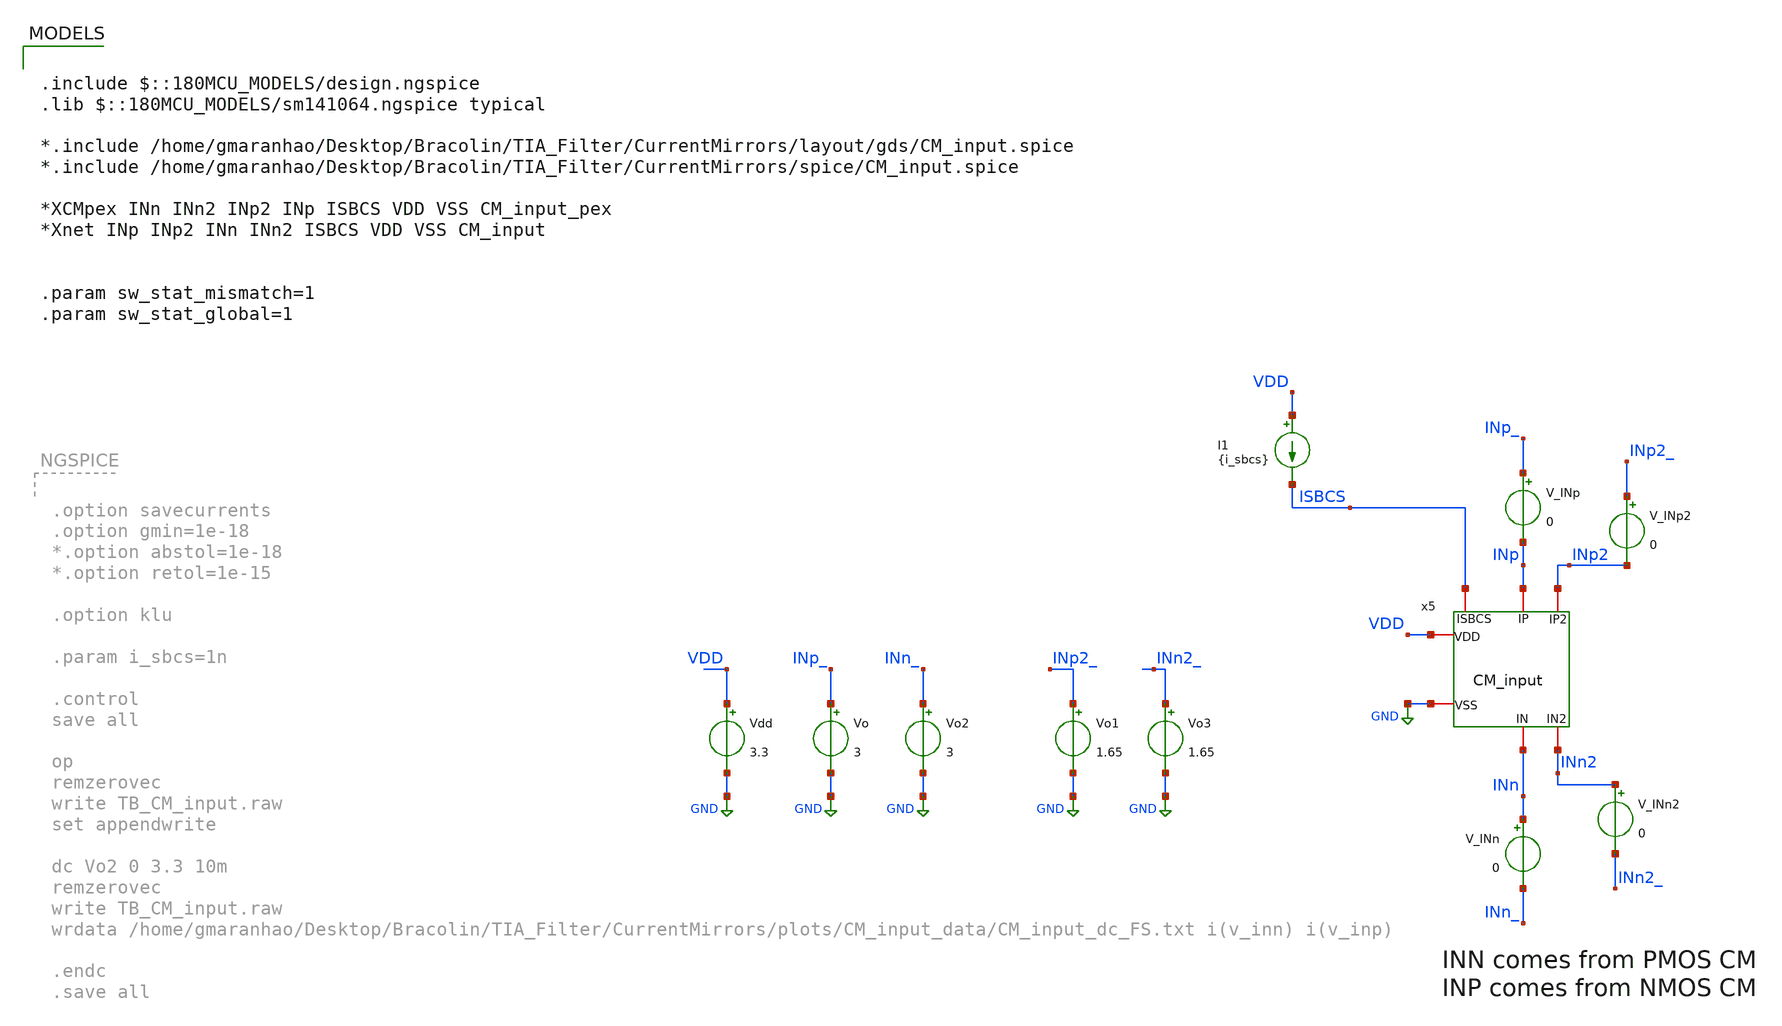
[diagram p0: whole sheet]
** sch_path: TIA_Filter/CurrentMirrors/TB_CM_input.sch
**.subckt TB_CM_input
I1 VDD ISBCS {i_sbcs}
x5 INp INp2 INn INn2 ISBCS VDD GND CM_input
Vdd VDD GND 3.3
Vo INp_ GND 3
Vo1 INp2_ GND 1.65
Vo2 INn_ GND 3
Vo3 INn2_ GND 1.65
V_INp INp_ INp 0
V_INp2 INp2_ INp2 0
V_INn INn INn_ 0
V_INn2 INn2 INn2_ 0
**** begin user architecture code

.include $::180MCU_MODELS/design.ngspice
.lib $::180MCU_MODELS/sm141064.ngspice typical

*.include /home/gmaranhao/Desktop/Bracolin/TIA_Filter/CurrentMirrors/layout/gds/CM_input.spice
*.include /home/gmaranhao/Desktop/Bracolin/TIA_Filter/CurrentMirrors/spice/CM_input.spice

*XCMpex INn INn2 INp2 INp ISBCS VDD VSS CM_input_pex
*Xnet INp INp2 INn INn2 ISBCS VDD VSS CM_input


.param sw_stat_mismatch=1
.param sw_stat_global=1




.option gmin=1e-15
*.option abstol=1e-18
*.option retol=1e-15

.option klu

.param i_sbcs=1n

.control
save all

let sample_num = 0

while sample_num<203
reset

*dc Vo 0 3.3 10m
op
remzerovec
write TB_CM_input.raw
wrdata
+ /home/gmaranhao/Desktop/Bracolin/TIA_Filter/CurrentMirrors/plots/CM_input_data/CM_input_dc_MisMC_3p0.txt i(v_inn) i(v_inp)
set appendwrite

let sample_num = sample_num + 1
end


.endc
.save all


**** end user architecture code
**.ends

* expanding   symbol:  CurrentMirrors/CM_input.sym # of pins=7
** sym_path: TIA_Filter/CurrentMirrors/CM_input.sym
** sch_path: TIA_Filter/CurrentMirrors/CM_input.sch
.subckt CM_input IP IP2 IN IN2 ISBCS VDD VSS
*.iopin IP
*.iopin IP2
*.iopin IN
*.iopin IN2
*.iopin ISBCS
*.iopin VDD
*.iopin VSS
XM1[1] ISBCS ISBCS net1[1] VSS nfet_03v3 L=6u W=2u nf=1 ad='int((nf+1)/2) * W/nf * 0.18u' as='int((nf+2)/2) * W/nf * 0.18u'
+ pd='2*int((nf+1)/2) * (W/nf + 0.18u)' ps='2*int((nf+2)/2) * (W/nf + 0.18u)' nrd='0.18u / W' nrs='0.18u / W'
+ sa=0 sb=0 sd=0 m=1
XM1[2] ISBCS ISBCS net1[0] VSS nfet_03v3 L=6u W=2u nf=1 ad='int((nf+1)/2) * W/nf * 0.18u' as='int((nf+2)/2) * W/nf * 0.18u'
+ pd='2*int((nf+1)/2) * (W/nf + 0.18u)' ps='2*int((nf+2)/2) * (W/nf + 0.18u)' nrd='0.18u / W' nrs='0.18u / W'
+ sa=0 sb=0 sd=0 m=1
XM2[1] vgp vgp net5[1] VDD pfet_03v3 L=6u W=2u nf=1 ad='int((nf+1)/2) * W/nf * 0.18u' as='int((nf+2)/2) * W/nf * 0.18u'
+ pd='2*int((nf+1)/2) * (W/nf + 0.18u)' ps='2*int((nf+2)/2) * (W/nf + 0.18u)' nrd='0.18u / W' nrs='0.18u / W'
+ sa=0 sb=0 sd=0 m=1
XM2[2] vgp vgp net5[0] VDD pfet_03v3 L=6u W=2u nf=1 ad='int((nf+1)/2) * W/nf * 0.18u' as='int((nf+2)/2) * W/nf * 0.18u'
+ pd='2*int((nf+1)/2) * (W/nf + 0.18u)' ps='2*int((nf+2)/2) * (W/nf + 0.18u)' nrd='0.18u / W' nrs='0.18u / W'
+ sa=0 sb=0 sd=0 m=1
XM3[1] net1[1] ISBCS VSS VSS nfet_03v3 L=6u W=2u nf=1 ad='int((nf+1)/2) * W/nf * 0.18u' as='int((nf+2)/2) * W/nf * 0.18u'
+ pd='2*int((nf+1)/2) * (W/nf + 0.18u)' ps='2*int((nf+2)/2) * (W/nf + 0.18u)' nrd='0.18u / W' nrs='0.18u / W'
+ sa=0 sb=0 sd=0 m=1
XM3[2] net1[0] ISBCS VSS VSS nfet_03v3 L=6u W=2u nf=1 ad='int((nf+1)/2) * W/nf * 0.18u' as='int((nf+2)/2) * W/nf * 0.18u'
+ pd='2*int((nf+1)/2) * (W/nf + 0.18u)' ps='2*int((nf+2)/2) * (W/nf + 0.18u)' nrd='0.18u / W' nrs='0.18u / W'
+ sa=0 sb=0 sd=0 m=1
XM4[1] IP ISBCS net2[1] VSS nfet_03v3 L=6u W=2u nf=1 ad='int((nf+1)/2) * W/nf * 0.18u' as='int((nf+2)/2) * W/nf * 0.18u'
+ pd='2*int((nf+1)/2) * (W/nf + 0.18u)' ps='2*int((nf+2)/2) * (W/nf + 0.18u)' nrd='0.18u / W' nrs='0.18u / W'
+ sa=0 sb=0 sd=0 m=1
XM4[2] IP ISBCS net2[0] VSS nfet_03v3 L=6u W=2u nf=1 ad='int((nf+1)/2) * W/nf * 0.18u' as='int((nf+2)/2) * W/nf * 0.18u'
+ pd='2*int((nf+1)/2) * (W/nf + 0.18u)' ps='2*int((nf+2)/2) * (W/nf + 0.18u)' nrd='0.18u / W' nrs='0.18u / W'
+ sa=0 sb=0 sd=0 m=1
XM5[1] net2[1] ISBCS VSS VSS nfet_03v3 L=6u W=2u nf=1 ad='int((nf+1)/2) * W/nf * 0.18u' as='int((nf+2)/2) * W/nf * 0.18u'
+ pd='2*int((nf+1)/2) * (W/nf + 0.18u)' ps='2*int((nf+2)/2) * (W/nf + 0.18u)' nrd='0.18u / W' nrs='0.18u / W'
+ sa=0 sb=0 sd=0 m=1
XM5[2] net2[0] ISBCS VSS VSS nfet_03v3 L=6u W=2u nf=1 ad='int((nf+1)/2) * W/nf * 0.18u' as='int((nf+2)/2) * W/nf * 0.18u'
+ pd='2*int((nf+1)/2) * (W/nf + 0.18u)' ps='2*int((nf+2)/2) * (W/nf + 0.18u)' nrd='0.18u / W' nrs='0.18u / W'
+ sa=0 sb=0 sd=0 m=1
XM6[1] IP2 ISBCS net3[1] VSS nfet_03v3 L=6u W=2u nf=1 ad='int((nf+1)/2) * W/nf * 0.18u' as='int((nf+2)/2) * W/nf * 0.18u'
+ pd='2*int((nf+1)/2) * (W/nf + 0.18u)' ps='2*int((nf+2)/2) * (W/nf + 0.18u)' nrd='0.18u / W' nrs='0.18u / W'
+ sa=0 sb=0 sd=0 m=1
XM6[2] IP2 ISBCS net3[0] VSS nfet_03v3 L=6u W=2u nf=1 ad='int((nf+1)/2) * W/nf * 0.18u' as='int((nf+2)/2) * W/nf * 0.18u'
+ pd='2*int((nf+1)/2) * (W/nf + 0.18u)' ps='2*int((nf+2)/2) * (W/nf + 0.18u)' nrd='0.18u / W' nrs='0.18u / W'
+ sa=0 sb=0 sd=0 m=1
XM7[1] net3[1] ISBCS VSS VSS nfet_03v3 L=6u W=2u nf=1 ad='int((nf+1)/2) * W/nf * 0.18u' as='int((nf+2)/2) * W/nf * 0.18u'
+ pd='2*int((nf+1)/2) * (W/nf + 0.18u)' ps='2*int((nf+2)/2) * (W/nf + 0.18u)' nrd='0.18u / W' nrs='0.18u / W'
+ sa=0 sb=0 sd=0 m=1
XM7[2] net3[0] ISBCS VSS VSS nfet_03v3 L=6u W=2u nf=1 ad='int((nf+1)/2) * W/nf * 0.18u' as='int((nf+2)/2) * W/nf * 0.18u'
+ pd='2*int((nf+1)/2) * (W/nf + 0.18u)' ps='2*int((nf+2)/2) * (W/nf + 0.18u)' nrd='0.18u / W' nrs='0.18u / W'
+ sa=0 sb=0 sd=0 m=1
XM8[1] vgp ISBCS net4[1] VSS nfet_03v3 L=6u W=2u nf=1 ad='int((nf+1)/2) * W/nf * 0.18u' as='int((nf+2)/2) * W/nf * 0.18u'
+ pd='2*int((nf+1)/2) * (W/nf + 0.18u)' ps='2*int((nf+2)/2) * (W/nf + 0.18u)' nrd='0.18u / W' nrs='0.18u / W'
+ sa=0 sb=0 sd=0 m=1
XM8[2] vgp ISBCS net4[0] VSS nfet_03v3 L=6u W=2u nf=1 ad='int((nf+1)/2) * W/nf * 0.18u' as='int((nf+2)/2) * W/nf * 0.18u'
+ pd='2*int((nf+1)/2) * (W/nf + 0.18u)' ps='2*int((nf+2)/2) * (W/nf + 0.18u)' nrd='0.18u / W' nrs='0.18u / W'
+ sa=0 sb=0 sd=0 m=1
XM9[1] net4[1] ISBCS VSS VSS nfet_03v3 L=6u W=2u nf=1 ad='int((nf+1)/2) * W/nf * 0.18u' as='int((nf+2)/2) * W/nf * 0.18u'
+ pd='2*int((nf+1)/2) * (W/nf + 0.18u)' ps='2*int((nf+2)/2) * (W/nf + 0.18u)' nrd='0.18u / W' nrs='0.18u / W'
+ sa=0 sb=0 sd=0 m=1
XM9[2] net4[0] ISBCS VSS VSS nfet_03v3 L=6u W=2u nf=1 ad='int((nf+1)/2) * W/nf * 0.18u' as='int((nf+2)/2) * W/nf * 0.18u'
+ pd='2*int((nf+1)/2) * (W/nf + 0.18u)' ps='2*int((nf+2)/2) * (W/nf + 0.18u)' nrd='0.18u / W' nrs='0.18u / W'
+ sa=0 sb=0 sd=0 m=1
XM10[1] net5[1] vgp VDD VDD pfet_03v3 L=6u W=2u nf=1 ad='int((nf+1)/2) * W/nf * 0.18u' as='int((nf+2)/2) * W/nf * 0.18u'
+ pd='2*int((nf+1)/2) * (W/nf + 0.18u)' ps='2*int((nf+2)/2) * (W/nf + 0.18u)' nrd='0.18u / W' nrs='0.18u / W'
+ sa=0 sb=0 sd=0 m=1
XM10[2] net5[0] vgp VDD VDD pfet_03v3 L=6u W=2u nf=1 ad='int((nf+1)/2) * W/nf * 0.18u' as='int((nf+2)/2) * W/nf * 0.18u'
+ pd='2*int((nf+1)/2) * (W/nf + 0.18u)' ps='2*int((nf+2)/2) * (W/nf + 0.18u)' nrd='0.18u / W' nrs='0.18u / W'
+ sa=0 sb=0 sd=0 m=1
XM11[1] IN vgp net6[1] VDD pfet_03v3 L=6u W=2u nf=1 ad='int((nf+1)/2) * W/nf * 0.18u' as='int((nf+2)/2) * W/nf * 0.18u'
+ pd='2*int((nf+1)/2) * (W/nf + 0.18u)' ps='2*int((nf+2)/2) * (W/nf + 0.18u)' nrd='0.18u / W' nrs='0.18u / W'
+ sa=0 sb=0 sd=0 m=1
XM11[2] IN vgp net6[0] VDD pfet_03v3 L=6u W=2u nf=1 ad='int((nf+1)/2) * W/nf * 0.18u' as='int((nf+2)/2) * W/nf * 0.18u'
+ pd='2*int((nf+1)/2) * (W/nf + 0.18u)' ps='2*int((nf+2)/2) * (W/nf + 0.18u)' nrd='0.18u / W' nrs='0.18u / W'
+ sa=0 sb=0 sd=0 m=1
XM12[1] net6[1] vgp VDD VDD pfet_03v3 L=6u W=2u nf=1 ad='int((nf+1)/2) * W/nf * 0.18u' as='int((nf+2)/2) * W/nf * 0.18u'
+ pd='2*int((nf+1)/2) * (W/nf + 0.18u)' ps='2*int((nf+2)/2) * (W/nf + 0.18u)' nrd='0.18u / W' nrs='0.18u / W'
+ sa=0 sb=0 sd=0 m=1
XM12[2] net6[0] vgp VDD VDD pfet_03v3 L=6u W=2u nf=1 ad='int((nf+1)/2) * W/nf * 0.18u' as='int((nf+2)/2) * W/nf * 0.18u'
+ pd='2*int((nf+1)/2) * (W/nf + 0.18u)' ps='2*int((nf+2)/2) * (W/nf + 0.18u)' nrd='0.18u / W' nrs='0.18u / W'
+ sa=0 sb=0 sd=0 m=1
XM13[1] IN2 vgp net7[1] VDD pfet_03v3 L=6u W=2u nf=1 ad='int((nf+1)/2) * W/nf * 0.18u' as='int((nf+2)/2) * W/nf * 0.18u'
+ pd='2*int((nf+1)/2) * (W/nf + 0.18u)' ps='2*int((nf+2)/2) * (W/nf + 0.18u)' nrd='0.18u / W' nrs='0.18u / W'
+ sa=0 sb=0 sd=0 m=1
XM13[2] IN2 vgp net7[0] VDD pfet_03v3 L=6u W=2u nf=1 ad='int((nf+1)/2) * W/nf * 0.18u' as='int((nf+2)/2) * W/nf * 0.18u'
+ pd='2*int((nf+1)/2) * (W/nf + 0.18u)' ps='2*int((nf+2)/2) * (W/nf + 0.18u)' nrd='0.18u / W' nrs='0.18u / W'
+ sa=0 sb=0 sd=0 m=1
XM16[1] net7[1] vgp VDD VDD pfet_03v3 L=6u W=2u nf=1 ad='int((nf+1)/2) * W/nf * 0.18u' as='int((nf+2)/2) * W/nf * 0.18u'
+ pd='2*int((nf+1)/2) * (W/nf + 0.18u)' ps='2*int((nf+2)/2) * (W/nf + 0.18u)' nrd='0.18u / W' nrs='0.18u / W'
+ sa=0 sb=0 sd=0 m=1
XM16[2] net7[0] vgp VDD VDD pfet_03v3 L=6u W=2u nf=1 ad='int((nf+1)/2) * W/nf * 0.18u' as='int((nf+2)/2) * W/nf * 0.18u'
+ pd='2*int((nf+1)/2) * (W/nf + 0.18u)' ps='2*int((nf+2)/2) * (W/nf + 0.18u)' nrd='0.18u / W' nrs='0.18u / W'
+ sa=0 sb=0 sd=0 m=1
XM14[1] VSS VSS VSS VSS nfet_03v3 L=6u W=2u nf=1 ad='int((nf+1)/2) * W/nf * 0.18u' as='int((nf+2)/2) * W/nf * 0.18u'
+ pd='2*int((nf+1)/2) * (W/nf + 0.18u)' ps='2*int((nf+2)/2) * (W/nf + 0.18u)' nrd='0.18u / W' nrs='0.18u / W'
+ sa=0 sb=0 sd=0 m=1
XM14[2] VSS VSS VSS VSS nfet_03v3 L=6u W=2u nf=1 ad='int((nf+1)/2) * W/nf * 0.18u' as='int((nf+2)/2) * W/nf * 0.18u'
+ pd='2*int((nf+1)/2) * (W/nf + 0.18u)' ps='2*int((nf+2)/2) * (W/nf + 0.18u)' nrd='0.18u / W' nrs='0.18u / W'
+ sa=0 sb=0 sd=0 m=1
XM14[3] VSS VSS VSS VSS nfet_03v3 L=6u W=2u nf=1 ad='int((nf+1)/2) * W/nf * 0.18u' as='int((nf+2)/2) * W/nf * 0.18u'
+ pd='2*int((nf+1)/2) * (W/nf + 0.18u)' ps='2*int((nf+2)/2) * (W/nf + 0.18u)' nrd='0.18u / W' nrs='0.18u / W'
+ sa=0 sb=0 sd=0 m=1
XM14[4] VSS VSS VSS VSS nfet_03v3 L=6u W=2u nf=1 ad='int((nf+1)/2) * W/nf * 0.18u' as='int((nf+2)/2) * W/nf * 0.18u'
+ pd='2*int((nf+1)/2) * (W/nf + 0.18u)' ps='2*int((nf+2)/2) * (W/nf + 0.18u)' nrd='0.18u / W' nrs='0.18u / W'
+ sa=0 sb=0 sd=0 m=1
XM14[5] VSS VSS VSS VSS nfet_03v3 L=6u W=2u nf=1 ad='int((nf+1)/2) * W/nf * 0.18u' as='int((nf+2)/2) * W/nf * 0.18u'
+ pd='2*int((nf+1)/2) * (W/nf + 0.18u)' ps='2*int((nf+2)/2) * (W/nf + 0.18u)' nrd='0.18u / W' nrs='0.18u / W'
+ sa=0 sb=0 sd=0 m=1
XM14[6] VSS VSS VSS VSS nfet_03v3 L=6u W=2u nf=1 ad='int((nf+1)/2) * W/nf * 0.18u' as='int((nf+2)/2) * W/nf * 0.18u'
+ pd='2*int((nf+1)/2) * (W/nf + 0.18u)' ps='2*int((nf+2)/2) * (W/nf + 0.18u)' nrd='0.18u / W' nrs='0.18u / W'
+ sa=0 sb=0 sd=0 m=1
XM14[7] VSS VSS VSS VSS nfet_03v3 L=6u W=2u nf=1 ad='int((nf+1)/2) * W/nf * 0.18u' as='int((nf+2)/2) * W/nf * 0.18u'
+ pd='2*int((nf+1)/2) * (W/nf + 0.18u)' ps='2*int((nf+2)/2) * (W/nf + 0.18u)' nrd='0.18u / W' nrs='0.18u / W'
+ sa=0 sb=0 sd=0 m=1
XM14[8] VSS VSS VSS VSS nfet_03v3 L=6u W=2u nf=1 ad='int((nf+1)/2) * W/nf * 0.18u' as='int((nf+2)/2) * W/nf * 0.18u'
+ pd='2*int((nf+1)/2) * (W/nf + 0.18u)' ps='2*int((nf+2)/2) * (W/nf + 0.18u)' nrd='0.18u / W' nrs='0.18u / W'
+ sa=0 sb=0 sd=0 m=1
XM14[9] VSS VSS VSS VSS nfet_03v3 L=6u W=2u nf=1 ad='int((nf+1)/2) * W/nf * 0.18u' as='int((nf+2)/2) * W/nf * 0.18u'
+ pd='2*int((nf+1)/2) * (W/nf + 0.18u)' ps='2*int((nf+2)/2) * (W/nf + 0.18u)' nrd='0.18u / W' nrs='0.18u / W'
+ sa=0 sb=0 sd=0 m=1
XM14[10] VSS VSS VSS VSS nfet_03v3 L=6u W=2u nf=1 ad='int((nf+1)/2) * W/nf * 0.18u' as='int((nf+2)/2) * W/nf * 0.18u'
+ pd='2*int((nf+1)/2) * (W/nf + 0.18u)' ps='2*int((nf+2)/2) * (W/nf + 0.18u)' nrd='0.18u / W' nrs='0.18u / W'
+ sa=0 sb=0 sd=0 m=1
XM14[11] VSS VSS VSS VSS nfet_03v3 L=6u W=2u nf=1 ad='int((nf+1)/2) * W/nf * 0.18u' as='int((nf+2)/2) * W/nf * 0.18u'
+ pd='2*int((nf+1)/2) * (W/nf + 0.18u)' ps='2*int((nf+2)/2) * (W/nf + 0.18u)' nrd='0.18u / W' nrs='0.18u / W'
+ sa=0 sb=0 sd=0 m=1
XM14[12] VSS VSS VSS VSS nfet_03v3 L=6u W=2u nf=1 ad='int((nf+1)/2) * W/nf * 0.18u' as='int((nf+2)/2) * W/nf * 0.18u'
+ pd='2*int((nf+1)/2) * (W/nf + 0.18u)' ps='2*int((nf+2)/2) * (W/nf + 0.18u)' nrd='0.18u / W' nrs='0.18u / W'
+ sa=0 sb=0 sd=0 m=1
XM14[13] VSS VSS VSS VSS nfet_03v3 L=6u W=2u nf=1 ad='int((nf+1)/2) * W/nf * 0.18u' as='int((nf+2)/2) * W/nf * 0.18u'
+ pd='2*int((nf+1)/2) * (W/nf + 0.18u)' ps='2*int((nf+2)/2) * (W/nf + 0.18u)' nrd='0.18u / W' nrs='0.18u / W'
+ sa=0 sb=0 sd=0 m=1
XM14[14] VSS VSS VSS VSS nfet_03v3 L=6u W=2u nf=1 ad='int((nf+1)/2) * W/nf * 0.18u' as='int((nf+2)/2) * W/nf * 0.18u'
+ pd='2*int((nf+1)/2) * (W/nf + 0.18u)' ps='2*int((nf+2)/2) * (W/nf + 0.18u)' nrd='0.18u / W' nrs='0.18u / W'
+ sa=0 sb=0 sd=0 m=1
XM14[15] VSS VSS VSS VSS nfet_03v3 L=6u W=2u nf=1 ad='int((nf+1)/2) * W/nf * 0.18u' as='int((nf+2)/2) * W/nf * 0.18u'
+ pd='2*int((nf+1)/2) * (W/nf + 0.18u)' ps='2*int((nf+2)/2) * (W/nf + 0.18u)' nrd='0.18u / W' nrs='0.18u / W'
+ sa=0 sb=0 sd=0 m=1
XM14[16] VSS VSS VSS VSS nfet_03v3 L=6u W=2u nf=1 ad='int((nf+1)/2) * W/nf * 0.18u' as='int((nf+2)/2) * W/nf * 0.18u'
+ pd='2*int((nf+1)/2) * (W/nf + 0.18u)' ps='2*int((nf+2)/2) * (W/nf + 0.18u)' nrd='0.18u / W' nrs='0.18u / W'
+ sa=0 sb=0 sd=0 m=1
XM14[17] VSS VSS VSS VSS nfet_03v3 L=6u W=2u nf=1 ad='int((nf+1)/2) * W/nf * 0.18u' as='int((nf+2)/2) * W/nf * 0.18u'
+ pd='2*int((nf+1)/2) * (W/nf + 0.18u)' ps='2*int((nf+2)/2) * (W/nf + 0.18u)' nrd='0.18u / W' nrs='0.18u / W'
+ sa=0 sb=0 sd=0 m=1
XM14[18] VSS VSS VSS VSS nfet_03v3 L=6u W=2u nf=1 ad='int((nf+1)/2) * W/nf * 0.18u' as='int((nf+2)/2) * W/nf * 0.18u'
+ pd='2*int((nf+1)/2) * (W/nf + 0.18u)' ps='2*int((nf+2)/2) * (W/nf + 0.18u)' nrd='0.18u / W' nrs='0.18u / W'
+ sa=0 sb=0 sd=0 m=1
XM14[19] VSS VSS VSS VSS nfet_03v3 L=6u W=2u nf=1 ad='int((nf+1)/2) * W/nf * 0.18u' as='int((nf+2)/2) * W/nf * 0.18u'
+ pd='2*int((nf+1)/2) * (W/nf + 0.18u)' ps='2*int((nf+2)/2) * (W/nf + 0.18u)' nrd='0.18u / W' nrs='0.18u / W'
+ sa=0 sb=0 sd=0 m=1
XM14[20] VSS VSS VSS VSS nfet_03v3 L=6u W=2u nf=1 ad='int((nf+1)/2) * W/nf * 0.18u' as='int((nf+2)/2) * W/nf * 0.18u'
+ pd='2*int((nf+1)/2) * (W/nf + 0.18u)' ps='2*int((nf+2)/2) * (W/nf + 0.18u)' nrd='0.18u / W' nrs='0.18u / W'
+ sa=0 sb=0 sd=0 m=1
XM15[1] VDD VDD VDD VDD pfet_03v3 L=6u W=2u nf=1 ad='int((nf+1)/2) * W/nf * 0.18u' as='int((nf+2)/2) * W/nf * 0.18u'
+ pd='2*int((nf+1)/2) * (W/nf + 0.18u)' ps='2*int((nf+2)/2) * (W/nf + 0.18u)' nrd='0.18u / W' nrs='0.18u / W'
+ sa=0 sb=0 sd=0 m=1
XM15[2] VDD VDD VDD VDD pfet_03v3 L=6u W=2u nf=1 ad='int((nf+1)/2) * W/nf * 0.18u' as='int((nf+2)/2) * W/nf * 0.18u'
+ pd='2*int((nf+1)/2) * (W/nf + 0.18u)' ps='2*int((nf+2)/2) * (W/nf + 0.18u)' nrd='0.18u / W' nrs='0.18u / W'
+ sa=0 sb=0 sd=0 m=1
XM15[3] VDD VDD VDD VDD pfet_03v3 L=6u W=2u nf=1 ad='int((nf+1)/2) * W/nf * 0.18u' as='int((nf+2)/2) * W/nf * 0.18u'
+ pd='2*int((nf+1)/2) * (W/nf + 0.18u)' ps='2*int((nf+2)/2) * (W/nf + 0.18u)' nrd='0.18u / W' nrs='0.18u / W'
+ sa=0 sb=0 sd=0 m=1
XM15[4] VDD VDD VDD VDD pfet_03v3 L=6u W=2u nf=1 ad='int((nf+1)/2) * W/nf * 0.18u' as='int((nf+2)/2) * W/nf * 0.18u'
+ pd='2*int((nf+1)/2) * (W/nf + 0.18u)' ps='2*int((nf+2)/2) * (W/nf + 0.18u)' nrd='0.18u / W' nrs='0.18u / W'
+ sa=0 sb=0 sd=0 m=1
XM15[5] VDD VDD VDD VDD pfet_03v3 L=6u W=2u nf=1 ad='int((nf+1)/2) * W/nf * 0.18u' as='int((nf+2)/2) * W/nf * 0.18u'
+ pd='2*int((nf+1)/2) * (W/nf + 0.18u)' ps='2*int((nf+2)/2) * (W/nf + 0.18u)' nrd='0.18u / W' nrs='0.18u / W'
+ sa=0 sb=0 sd=0 m=1
XM15[6] VDD VDD VDD VDD pfet_03v3 L=6u W=2u nf=1 ad='int((nf+1)/2) * W/nf * 0.18u' as='int((nf+2)/2) * W/nf * 0.18u'
+ pd='2*int((nf+1)/2) * (W/nf + 0.18u)' ps='2*int((nf+2)/2) * (W/nf + 0.18u)' nrd='0.18u / W' nrs='0.18u / W'
+ sa=0 sb=0 sd=0 m=1
XM15[7] VDD VDD VDD VDD pfet_03v3 L=6u W=2u nf=1 ad='int((nf+1)/2) * W/nf * 0.18u' as='int((nf+2)/2) * W/nf * 0.18u'
+ pd='2*int((nf+1)/2) * (W/nf + 0.18u)' ps='2*int((nf+2)/2) * (W/nf + 0.18u)' nrd='0.18u / W' nrs='0.18u / W'
+ sa=0 sb=0 sd=0 m=1
XM15[8] VDD VDD VDD VDD pfet_03v3 L=6u W=2u nf=1 ad='int((nf+1)/2) * W/nf * 0.18u' as='int((nf+2)/2) * W/nf * 0.18u'
+ pd='2*int((nf+1)/2) * (W/nf + 0.18u)' ps='2*int((nf+2)/2) * (W/nf + 0.18u)' nrd='0.18u / W' nrs='0.18u / W'
+ sa=0 sb=0 sd=0 m=1
XM15[9] VDD VDD VDD VDD pfet_03v3 L=6u W=2u nf=1 ad='int((nf+1)/2) * W/nf * 0.18u' as='int((nf+2)/2) * W/nf * 0.18u'
+ pd='2*int((nf+1)/2) * (W/nf + 0.18u)' ps='2*int((nf+2)/2) * (W/nf + 0.18u)' nrd='0.18u / W' nrs='0.18u / W'
+ sa=0 sb=0 sd=0 m=1
XM15[10] VDD VDD VDD VDD pfet_03v3 L=6u W=2u nf=1 ad='int((nf+1)/2) * W/nf * 0.18u' as='int((nf+2)/2) * W/nf * 0.18u'
+ pd='2*int((nf+1)/2) * (W/nf + 0.18u)' ps='2*int((nf+2)/2) * (W/nf + 0.18u)' nrd='0.18u / W' nrs='0.18u / W'
+ sa=0 sb=0 sd=0 m=1
XM15[11] VDD VDD VDD VDD pfet_03v3 L=6u W=2u nf=1 ad='int((nf+1)/2) * W/nf * 0.18u' as='int((nf+2)/2) * W/nf * 0.18u'
+ pd='2*int((nf+1)/2) * (W/nf + 0.18u)' ps='2*int((nf+2)/2) * (W/nf + 0.18u)' nrd='0.18u / W' nrs='0.18u / W'
+ sa=0 sb=0 sd=0 m=1
XM15[12] VDD VDD VDD VDD pfet_03v3 L=6u W=2u nf=1 ad='int((nf+1)/2) * W/nf * 0.18u' as='int((nf+2)/2) * W/nf * 0.18u'
+ pd='2*int((nf+1)/2) * (W/nf + 0.18u)' ps='2*int((nf+2)/2) * (W/nf + 0.18u)' nrd='0.18u / W' nrs='0.18u / W'
+ sa=0 sb=0 sd=0 m=1
XM15[13] VDD VDD VDD VDD pfet_03v3 L=6u W=2u nf=1 ad='int((nf+1)/2) * W/nf * 0.18u' as='int((nf+2)/2) * W/nf * 0.18u'
+ pd='2*int((nf+1)/2) * (W/nf + 0.18u)' ps='2*int((nf+2)/2) * (W/nf + 0.18u)' nrd='0.18u / W' nrs='0.18u / W'
+ sa=0 sb=0 sd=0 m=1
XM15[14] VDD VDD VDD VDD pfet_03v3 L=6u W=2u nf=1 ad='int((nf+1)/2) * W/nf * 0.18u' as='int((nf+2)/2) * W/nf * 0.18u'
+ pd='2*int((nf+1)/2) * (W/nf + 0.18u)' ps='2*int((nf+2)/2) * (W/nf + 0.18u)' nrd='0.18u / W' nrs='0.18u / W'
+ sa=0 sb=0 sd=0 m=1
XM15[15] VDD VDD VDD VDD pfet_03v3 L=6u W=2u nf=1 ad='int((nf+1)/2) * W/nf * 0.18u' as='int((nf+2)/2) * W/nf * 0.18u'
+ pd='2*int((nf+1)/2) * (W/nf + 0.18u)' ps='2*int((nf+2)/2) * (W/nf + 0.18u)' nrd='0.18u / W' nrs='0.18u / W'
+ sa=0 sb=0 sd=0 m=1
XM15[16] VDD VDD VDD VDD pfet_03v3 L=6u W=2u nf=1 ad='int((nf+1)/2) * W/nf * 0.18u' as='int((nf+2)/2) * W/nf * 0.18u'
+ pd='2*int((nf+1)/2) * (W/nf + 0.18u)' ps='2*int((nf+2)/2) * (W/nf + 0.18u)' nrd='0.18u / W' nrs='0.18u / W'
+ sa=0 sb=0 sd=0 m=1
XM15[17] VDD VDD VDD VDD pfet_03v3 L=6u W=2u nf=1 ad='int((nf+1)/2) * W/nf * 0.18u' as='int((nf+2)/2) * W/nf * 0.18u'
+ pd='2*int((nf+1)/2) * (W/nf + 0.18u)' ps='2*int((nf+2)/2) * (W/nf + 0.18u)' nrd='0.18u / W' nrs='0.18u / W'
+ sa=0 sb=0 sd=0 m=1
XM15[18] VDD VDD VDD VDD pfet_03v3 L=6u W=2u nf=1 ad='int((nf+1)/2) * W/nf * 0.18u' as='int((nf+2)/2) * W/nf * 0.18u'
+ pd='2*int((nf+1)/2) * (W/nf + 0.18u)' ps='2*int((nf+2)/2) * (W/nf + 0.18u)' nrd='0.18u / W' nrs='0.18u / W'
+ sa=0 sb=0 sd=0 m=1
.ends

.GLOBAL GND
.end
